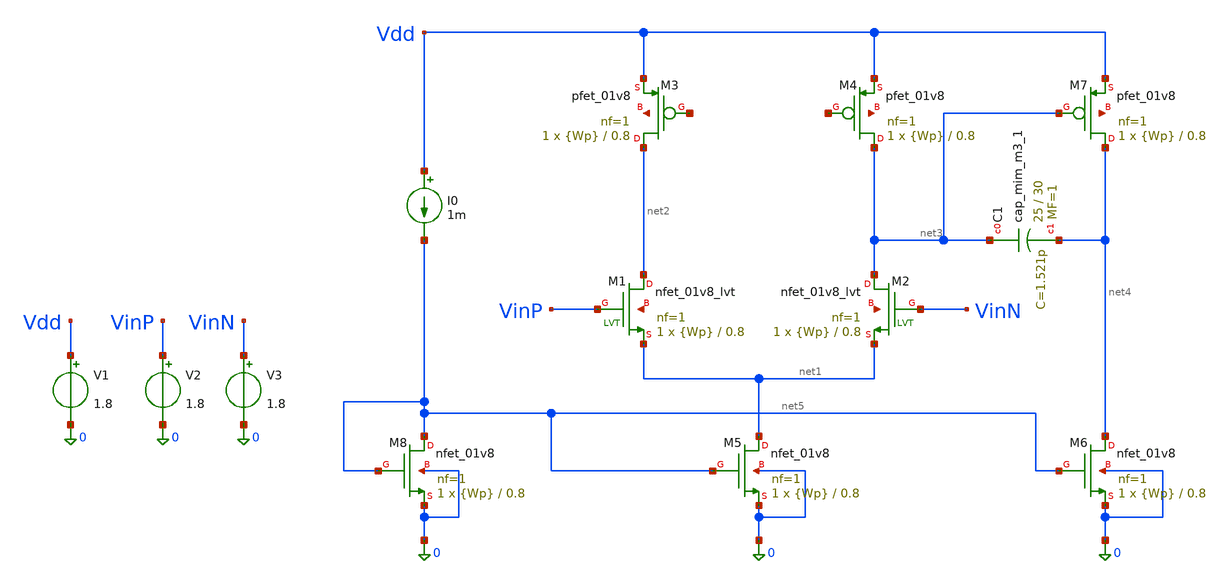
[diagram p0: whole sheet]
** sch_path: parameter_extraction/untitled.sch
**.subckt untitled
XM1 net2 VinP net1 net6 sky130_fd_pr__nfet_01v8_lvt L=0.8 W={Wp} nf=1 ad='int((1 + 1)/2) * {Wp} / 1 * 0.29'
+ as='int((1 + 2)/2) * {Wp} / 1 * 0.29' pd='2*int((1 + 1)/2) * ({Wp} / 1 + 0.29)' ps='2*int((1 + 2)/2) * ({Wp} / 1 + 0.29)'
+ nrd='0.29 / {Wp} ' nrs='0.29 / {Wp} ' sa=0 sb=0 sd=0 mult=1 m=1
XM3 net2 net7 Vdd net8 sky130_fd_pr__pfet_01v8 L=0.8 W={Wp} nf=1 ad='int((1 + 1)/2) * {Wp} / 1 * 0.29'
+ as='int((1 + 2)/2) * {Wp} / 1 * 0.29' pd='2*int((1 + 1)/2) * ({Wp} / 1 + 0.29)' ps='2*int((1 + 2)/2) * ({Wp} / 1 + 0.29)'
+ nrd='0.29 / {Wp} ' nrs='0.29 / {Wp} ' sa=0 sb=0 sd=0 mult=1 m=1
XM5 net1 net5 0 0 sky130_fd_pr__nfet_01v8 L=0.8 W={Wp} nf=1 ad='int((1 + 1)/2) * {Wp} / 1 * 0.29' as='int((1 + 2)/2) * {Wp} / 1 * 0.29'
+ pd='2*int((1 + 1)/2) * ({Wp} / 1 + 0.29)' ps='2*int((1 + 2)/2) * ({Wp} / 1 + 0.29)' nrd='0.29 / {Wp} '
+ nrs='0.29 / {Wp} ' sa=0 sb=0 sd=0 mult=1 m=1
XM2 net3 VinN net1 net9 sky130_fd_pr__nfet_01v8_lvt L=0.8 W={Wp} nf=1 ad='int((1 + 1)/2) * {Wp} / 1 * 0.29'
+ as='int((1 + 2)/2) * {Wp} / 1 * 0.29' pd='2*int((1 + 1)/2) * ({Wp} / 1 + 0.29)' ps='2*int((1 + 2)/2) * ({Wp} / 1 + 0.29)'
+ nrd='0.29 / {Wp} ' nrs='0.29 / {Wp} ' sa=0 sb=0 sd=0 mult=1 m=1
XM4 net3 net10 Vdd net11 sky130_fd_pr__pfet_01v8 L=0.8 W={Wp} nf=1 ad='int((1 + 1)/2) * {Wp} / 1 * 0.29'
+ as='int((1 + 2)/2) * {Wp} / 1 * 0.29' pd='2*int((1 + 1)/2) * ({Wp} / 1 + 0.29)' ps='2*int((1 + 2)/2) * ({Wp} / 1 + 0.29)'
+ nrd='0.29 / {Wp} ' nrs='0.29 / {Wp} ' sa=0 sb=0 sd=0 mult=1 m=1
XM6 net4 net5 0 0 sky130_fd_pr__nfet_01v8 L=0.8 W={Wp} nf=1 ad='int((1 + 1)/2) * {Wp} / 1 * 0.29' as='int((1 + 2)/2) * {Wp} / 1 * 0.29'
+ pd='2*int((1 + 1)/2) * ({Wp} / 1 + 0.29)' ps='2*int((1 + 2)/2) * ({Wp} / 1 + 0.29)' nrd='0.29 / {Wp} '
+ nrs='0.29 / {Wp} ' sa=0 sb=0 sd=0 mult=1 m=1
XM7 net4 net3 Vdd net12 sky130_fd_pr__pfet_01v8 L=0.8 W={Wp} nf=1 ad='int((1 + 1)/2) * {Wp} / 1 * 0.29'
+ as='int((1 + 2)/2) * {Wp} / 1 * 0.29' pd='2*int((1 + 1)/2) * ({Wp} / 1 + 0.29)' ps='2*int((1 + 2)/2) * ({Wp} / 1 + 0.29)'
+ nrd='0.29 / {Wp} ' nrs='0.29 / {Wp} ' sa=0 sb=0 sd=0 mult=1 m=1
XC1 net3 net4 sky130_fd_pr__cap_mim_m3_1 W=25 L=30 MF=1 m=1
XM8 net5 net5 0 0 sky130_fd_pr__nfet_01v8 L=0.8 W={Wp} nf=1 ad='int((1 + 1)/2) * {Wp} / 1 * 0.29' as='int((1 + 2)/2) * {Wp} / 1 * 0.29'
+ pd='2*int((1 + 1)/2) * ({Wp} / 1 + 0.29)' ps='2*int((1 + 2)/2) * ({Wp} / 1 + 0.29)' nrd='0.29 / {Wp} '
+ nrs='0.29 / {Wp} ' sa=0 sb=0 sd=0 mult=1 m=1
V1 Vdd 0 1.8
I0 Vdd net5 1m
V2 VinP 0 1.8
V3 VinN 0 1.8
**.ends
.end
